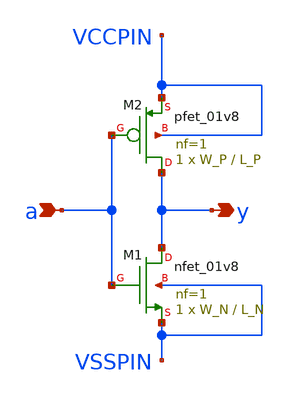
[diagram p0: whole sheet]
** sch_path: pdks/sky130A-1.0.227.01/libs.tech/xschem/sky130_tests/not.sch
* Copyright 2021 Stefan Frederik Schippers
* Licensed under the Apache License, Version 2.0 (the "License");
* you may not use this file except in compliance with the License.
* You may obtain a copy of the License at
* https://www.apache.org/licenses/LICENSE-2.0
* Unless required by applicable law or agreed to in writing, software
* distributed under the License is distributed on an "AS IS" BASIS,
* WITHOUT WARRANTIES OR CONDITIONS OF ANY KIND, either express or implied.
* See the License for the specific language governing permissions and
* limitations under the License.
**.subckt not y a
*.opin y
*.ipin a
XM1 y a VSSPIN VSSPIN sky130_fd_pr__nfet_01v8 L=L_N W=W_N nf=1 ad='int((1 + 1)/2) * W_N / 1 * 0.29' as='int((1 + 2)/2) * W_N / 1 * 0.29'
+ pd='2*int((1 + 1)/2) * (W_N / 1 + 0.29)' ps='2*int((1 + 2)/2) * (W_N / 1 + 0.29)' nrd='0.29 / W_N ' nrs='0.29 / W_N '
+ sa=0 sb=0 sd=0 mult=1 m=1
XM2 y a VCCPIN VCCPIN sky130_fd_pr__pfet_01v8 L=L_P W=W_P nf=1 ad='int((nf+1)/2) * W/nf * 0.29' as='int((nf+2)/2) * W/nf * 0.29'
+ pd='2*int((nf+1)/2) * (W/nf + 0.29)' ps='2*int((nf+2)/2) * (W/nf + 0.29)' nrd='0.29 / W' nrs='0.29 / W'
+ sa=0 sb=0 sd=0 mult=1 m=1
**** begin user architecture code

.lib $::SKYWATER_MODELS/sky130.lib.spice tt

**** end user architecture code
**.ends
.end
